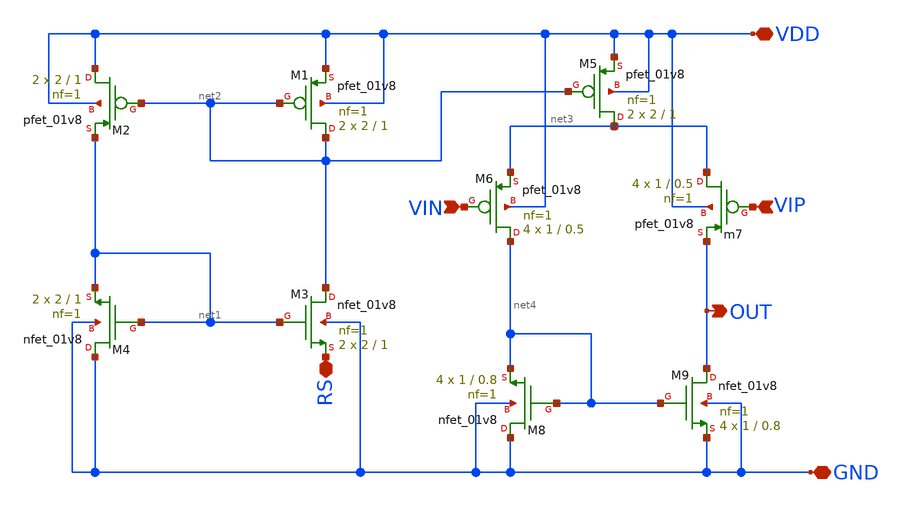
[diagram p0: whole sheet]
** sch_path: opamp/mag/opamp.sch
**.subckt opamp VDD VIN VIP OUT GND RS
*.iopin VDD
*.ipin VIN
*.ipin VIP
*.opin OUT
*.iopin GND
*.iopin RS
XM1 net2 net2 VDD VDD sky130_fd_pr__pfet_01v8 L=1 W=2 nf=1 ad='int((nf+1)/2) * W/nf * 0.29' as='int((nf+2)/2) * W/nf * 0.29'
+ pd='2*int((nf+1)/2) * (W/nf + 0.29)' ps='2*int((nf+2)/2) * (W/nf + 0.29)' nrd='0.29 / W' nrs='0.29 / W'
+ sa=0 sb=0 sd=0 mult=2 m=2
XM2 VDD net2 net1 VDD sky130_fd_pr__pfet_01v8 L=1 W=2 nf=1 ad='int((nf+1)/2) * W/nf * 0.29' as='int((nf+2)/2) * W/nf * 0.29'
+ pd='2*int((nf+1)/2) * (W/nf + 0.29)' ps='2*int((nf+2)/2) * (W/nf + 0.29)' nrd='0.29 / W' nrs='0.29 / W'
+ sa=0 sb=0 sd=0 mult=2 m=2
XM3 net2 net1 RS GND sky130_fd_pr__nfet_01v8 L=1 W=2 nf=1 ad='int((nf+1)/2) * W/nf * 0.29' as='int((nf+2)/2) * W/nf * 0.29'
+ pd='2*int((nf+1)/2) * (W/nf + 0.29)' ps='2*int((nf+2)/2) * (W/nf + 0.29)' nrd='0.29 / W' nrs='0.29 / W'
+ sa=0 sb=0 sd=0 mult=2 m=2
XM4 GND net1 net1 GND sky130_fd_pr__nfet_01v8 L=1 W=2 nf=1 ad='int((nf+1)/2) * W/nf * 0.29' as='int((nf+2)/2) * W/nf * 0.29'
+ pd='2*int((nf+1)/2) * (W/nf + 0.29)' ps='2*int((nf+2)/2) * (W/nf + 0.29)' nrd='0.29 / W' nrs='0.29 / W'
+ sa=0 sb=0 sd=0 mult=2 m=2
Xm7 net3 VIP OUT VDD sky130_fd_pr__pfet_01v8 L=0.5 W=1 nf=1 ad='int((nf+1)/2) * W/nf * 0.29' as='int((nf+2)/2) * W/nf * 0.29'
+ pd='2*int((nf+1)/2) * (W/nf + 0.29)' ps='2*int((nf+2)/2) * (W/nf + 0.29)' nrd='0.29 / W' nrs='0.29 / W'
+ sa=0 sb=0 sd=0 mult=4 m=4
XM6 net4 VIN net3 VDD sky130_fd_pr__pfet_01v8 L=0.5 W=1 nf=1 ad='int((nf+1)/2) * W/nf * 0.29' as='int((nf+2)/2) * W/nf * 0.29'
+ pd='2*int((nf+1)/2) * (W/nf + 0.29)' ps='2*int((nf+2)/2) * (W/nf + 0.29)' nrd='0.29 / W' nrs='0.29 / W'
+ sa=0 sb=0 sd=0 mult=4 m=4
XM9 OUT net4 GND GND sky130_fd_pr__nfet_01v8 L=0.8 W=1 nf=1 ad='int((nf+1)/2) * W/nf * 0.29' as='int((nf+2)/2) * W/nf * 0.29'
+ pd='2*int((nf+1)/2) * (W/nf + 0.29)' ps='2*int((nf+2)/2) * (W/nf + 0.29)' nrd='0.29 / W' nrs='0.29 / W'
+ sa=0 sb=0 sd=0 mult=4 m=4
XM8 GND net4 net4 GND sky130_fd_pr__nfet_01v8 L=0.8 W=1 nf=1 ad='int((nf+1)/2) * W/nf * 0.29' as='int((nf+2)/2) * W/nf * 0.29'
+ pd='2*int((nf+1)/2) * (W/nf + 0.29)' ps='2*int((nf+2)/2) * (W/nf + 0.29)' nrd='0.29 / W' nrs='0.29 / W'
+ sa=0 sb=0 sd=0 mult=4 m=4
XM5 net3 net2 VDD VDD sky130_fd_pr__pfet_01v8 L=1 W=2 nf=1 ad='int((nf+1)/2) * W/nf * 0.29' as='int((nf+2)/2) * W/nf * 0.29'
+ pd='2*int((nf+1)/2) * (W/nf + 0.29)' ps='2*int((nf+2)/2) * (W/nf + 0.29)' nrd='0.29 / W' nrs='0.29 / W'
+ sa=0 sb=0 sd=0 mult=2 m=2
**.ends
.end
